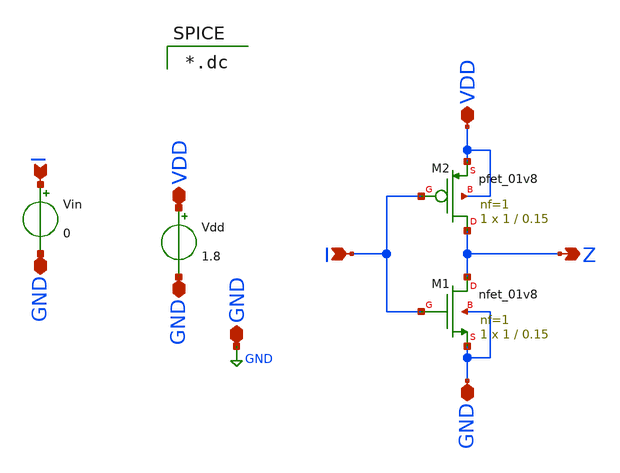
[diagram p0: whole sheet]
** sch_path: sky130_cells/Practice/Example_Inverter/Test_Example_Inverter.sch
**.subckt Test_Example_Inverter I Z VDD GND GND GND VDD GND I
*.ipin I
*.opin Z
*.iopin VDD
*.iopin GND
*.iopin GND
*.iopin GND
*.iopin VDD
*.iopin GND
*.ipin I
XM1 Z I GND GND sky130_fd_pr__nfet_01v8 L=0.15 W=1 nf=1 ad='int((nf+1)/2) * W/nf * 0.29' as='int((nf+2)/2) * W/nf * 0.29'
+ pd='2*int((nf+1)/2) * (W/nf + 0.29)' ps='2*int((nf+2)/2) * (W/nf + 0.29)' nrd='0.29 / W' nrs='0.29 / W'
+ sa=0 sb=0 sd=0 mult=1 m=1
XM2 Z I VDD VDD sky130_fd_pr__pfet_01v8 L=0.15 W=1 nf=1 ad='int((nf+1)/2) * W/nf * 0.29' as='int((nf+2)/2) * W/nf * 0.29'
+ pd='2*int((nf+1)/2) * (W/nf + 0.29)' ps='2*int((nf+2)/2) * (W/nf + 0.29)' nrd='0.29 / W' nrs='0.29 / W'
+ sa=0 sb=0 sd=0 mult=1 m=1
Vdd VDD GND 1.8
Vin I GND 0
**** begin user architecture code

*.dc

**** end user architecture code
**.ends
.GLOBAL GND
.end
